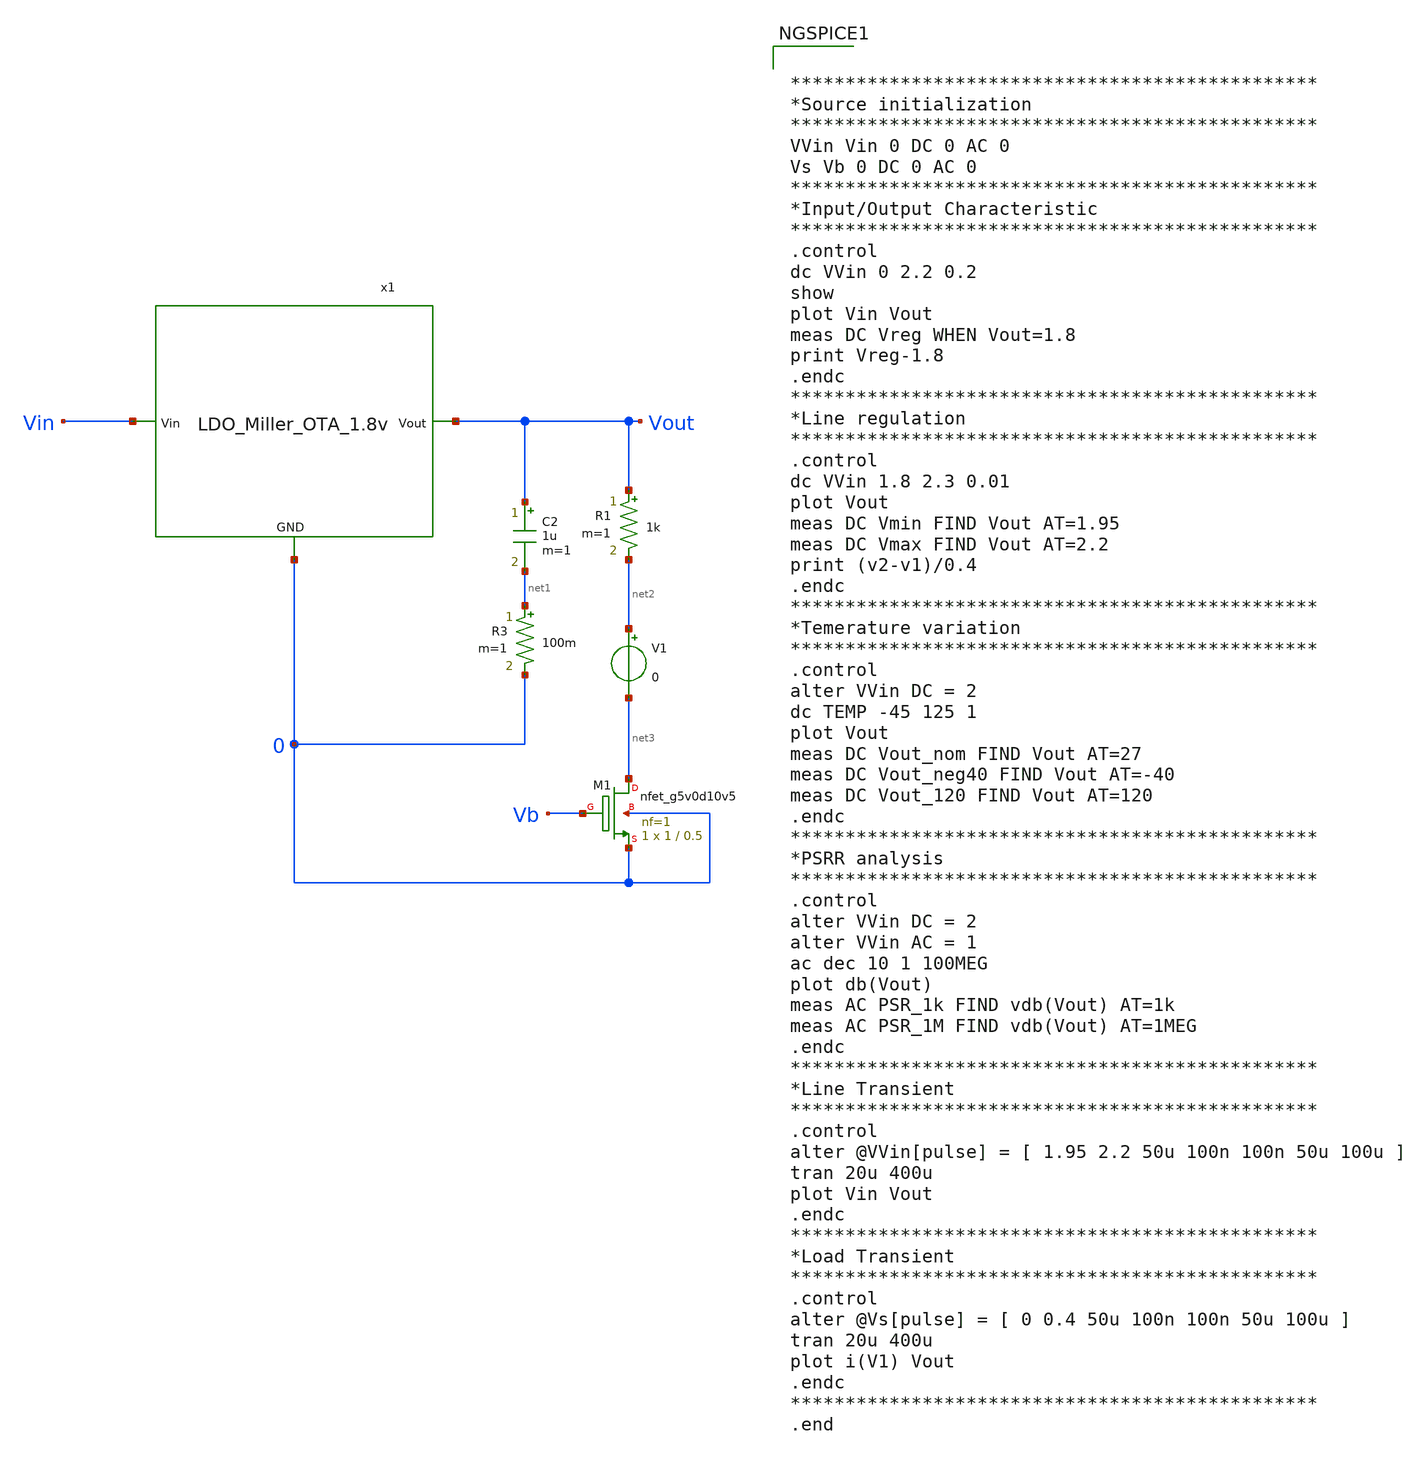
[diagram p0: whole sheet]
** sch_path: Analog_Blocks/LDO/Testbench/LDO_Miller_1.8v_meas.sch
**.subckt LDO_Miller_1.8v_meas
C2 Vout net1 1u m=1
R3 net1 0 100m m=1
x1 Vin Vout 0 LDO_Miller_OTA_1.8v
R1 Vout net2 1k m=1
XM1 net3 Vb 0 0 sky130_fd_pr__nfet_g5v0d10v5 L=0.5 W=1 nf=1 ad='int((nf+1)/2) * W/nf * 0.29' as='int((nf+2)/2) * W/nf * 0.29'
+ pd='2*int((nf+1)/2) * (W/nf + 0.29)' ps='2*int((nf+2)/2) * (W/nf + 0.29)' nrd='0.29 / W' nrs='0.29 / W'
+ sa=0 sb=0 sd=0 mult=1 m=1
V1 net2 net3 0
**** begin user architecture code


************************************************
*Source initialization
************************************************
VVin Vin 0 DC 0 AC 0
Vs Vb 0 DC 0 AC 0
************************************************
*Input/Output Characteristic
************************************************
.control
dc VVin 0 2.2 0.2
show
plot Vin Vout
meas DC Vreg WHEN Vout=1.8
print Vreg-1.8
.endc
************************************************
*Line regulation
************************************************
.control
dc VVin 1.8 2.3 0.01
plot Vout
meas DC Vmin FIND Vout AT=1.95
meas DC Vmax FIND Vout AT=2.2
print (v2-v1)/0.4
.endc
************************************************
*Temerature variation
************************************************
.control
alter VVin DC = 2
dc TEMP -45 125 1
plot Vout
meas DC Vout_nom FIND Vout AT=27
meas DC Vout_neg40 FIND Vout AT=-40
meas DC Vout_120 FIND Vout AT=120
.endc
************************************************
*PSRR analysis
************************************************
.control
alter VVin DC = 2
alter VVin AC = 1
ac dec 10 1 100MEG
plot db(Vout)
meas AC PSR_1k FIND vdb(Vout) AT=1k
meas AC PSR_1M FIND vdb(Vout) AT=1MEG
.endc
************************************************
*Line Transient
************************************************
.control
alter @VVin[pulse] = [ 1.95 2.2 50u 100n 100n 50u 100u ]
tran 20u 400u
plot Vin Vout
.endc
************************************************
*Load Transient
************************************************
.control
alter @Vs[pulse] = [ 0 0.4 50u 100n 100n 50u 100u ]
tran 20u 400u
plot i(V1) Vout
.endc
************************************************
.end



.include ~/Analog_blocks/models/skywater-pdk/libraries/sky130_fd_pr/latest/cells/nfet_01v8/sky130_fd_pr__nfet_01v8__tt.corner.spice
.include ~/Analog_blocks/models/skywater-pdk/libraries/sky130_fd_pr/latest/cells/nfet_01v8_lvt/sky130_fd_pr__nfet_01v8_lvt__tt.corner.spice
.include ~/Analog_blocks/models/skywater-pdk/libraries/sky130_fd_pr/latest/cells/pfet_01v8/sky130_fd_pr__pfet_01v8__tt.corner.spice
.include ~/Analog_blocks/models/skywater-pdk/libraries/sky130_fd_pr/latest/cells/nfet_03v3_nvt/sky130_fd_pr__nfet_03v3_nvt__tt.corner.spice
.include ~/Analog_blocks/models/skywater-pdk/libraries/sky130_fd_pr/latest/cells/nfet_05v0_nvt/sky130_fd_pr__nfet_05v0_nvt__tt.corner.spice
.include ~/Analog_blocks/models/skywater-pdk/libraries/sky130_fd_pr/latest/cells/esd_nfet_01v8/sky130_fd_pr__esd_nfet_01v8__tt.corner.spice
.include ~/Analog_blocks/models/skywater-pdk/libraries/sky130_fd_pr/latest/cells/pfet_01v8_lvt/sky130_fd_pr__pfet_01v8_lvt__tt.corner.spice
.include ~/Analog_blocks/models/skywater-pdk/libraries/sky130_fd_pr/latest/cells/pfet_01v8_hvt/sky130_fd_pr__pfet_01v8_hvt__tt.corner.spice
.include ~/Analog_blocks/models/skywater-pdk/libraries/sky130_fd_pr/latest/cells/esd_pfet_g5v0d10v5/sky130_fd_pr__esd_pfet_g5v0d10v5__tt.corner.spice
.include ~/Analog_blocks/models/skywater-pdk/libraries/sky130_fd_pr/latest/cells/pfet_g5v0d10v5/sky130_fd_pr__pfet_g5v0d10v5__tt.corner.spice
.include ~/Analog_blocks/models/skywater-pdk/libraries/sky130_fd_pr/latest/cells/pfet_g5v0d16v0/sky130_fd_pr__pfet_g5v0d16v0__tt.corner.spice
.include ~/Analog_blocks/models/skywater-pdk/libraries/sky130_fd_pr/latest/cells/nfet_g5v0d10v5/sky130_fd_pr__nfet_g5v0d10v5__tt.corner.spice
.include ~/Analog_blocks/models/skywater-pdk/libraries/sky130_fd_pr/latest/cells/nfet_g5v0d16v0/sky130_fd_pr__nfet_g5v0d16v0__tt_discrete.corner.spice
.include ~/Analog_blocks/models/skywater-pdk/libraries/sky130_fd_pr/latest/cells/esd_nfet_g5v0d10v5/sky130_fd_pr__esd_nfet_g5v0d10v5__tt.corner.spice
.include ~/Analog_blocks/models/skywater-pdk/libraries/sky130_fd_pr/latest/models/corners/tt/nonfet.spice
* Mismatch parameters
.include ~/Analog_blocks/models/skywater-pdk/libraries/sky130_fd_pr/latest/cells/nfet_01v8/sky130_fd_pr__nfet_01v8__mismatch.corner.spice
.include ~/Analog_blocks/models/skywater-pdk/libraries/sky130_fd_pr/latest/cells/pfet_01v8/sky130_fd_pr__pfet_01v8__mismatch.corner.spice
.include ~/Analog_blocks/models/skywater-pdk/libraries/sky130_fd_pr/latest/cells/nfet_01v8_lvt/sky130_fd_pr__nfet_01v8_lvt__mismatch.corner.spice
.include ~/Analog_blocks/models/skywater-pdk/libraries/sky130_fd_pr/latest/cells/pfet_01v8_lvt/sky130_fd_pr__pfet_01v8_lvt__mismatch.corner.spice
.include ~/Analog_blocks/models/skywater-pdk/libraries/sky130_fd_pr/latest/cells/pfet_01v8_hvt/sky130_fd_pr__pfet_01v8_hvt__mismatch.corner.spice
.include ~/Analog_blocks/models/skywater-pdk/libraries/sky130_fd_pr/latest/cells/nfet_g5v0d10v5/sky130_fd_pr__nfet_g5v0d10v5__mismatch.corner.spice
.include ~/Analog_blocks/models/skywater-pdk/libraries/sky130_fd_pr/latest/cells/pfet_g5v0d10v5/sky130_fd_pr__pfet_g5v0d10v5__mismatch.corner.spice
.include ~/Analog_blocks/models/skywater-pdk/libraries/sky130_fd_pr/latest/cells/nfet_05v0_nvt/sky130_fd_pr__nfet_05v0_nvt__mismatch.corner.spice
.include ~/Analog_blocks/models/skywater-pdk/libraries/sky130_fd_pr/latest/cells/nfet_03v3_nvt/sky130_fd_pr__nfet_03v3_nvt__mismatch.corner.spice
* Resistor
.include ~/Analog_blocks/models/skywater-pdk/libraries/sky130_fd_pr/latest/models/r+c/res_typical__cap_typical.spice
.include ~/Analog_blocks/models/skywater-pdk/libraries/sky130_fd_pr/latest/models/r+c/res_typical__cap_typical__lin.spice
* Special cells
.include ~/Analog_blocks/models/skywater-pdk/libraries/sky130_fd_pr/latest/models/corners/tt/specialized_cells.spice
* All models
.include ~/Analog_blocks/models/skywater-pdk/libraries/sky130_fd_pr/latest/models/all.spice
* Corner
.include ~/Analog_blocks/models/skywater-pdk/libraries/sky130_fd_pr/latest/models/corners/tt/rf.spice

**** end user architecture code
**.ends
.end
